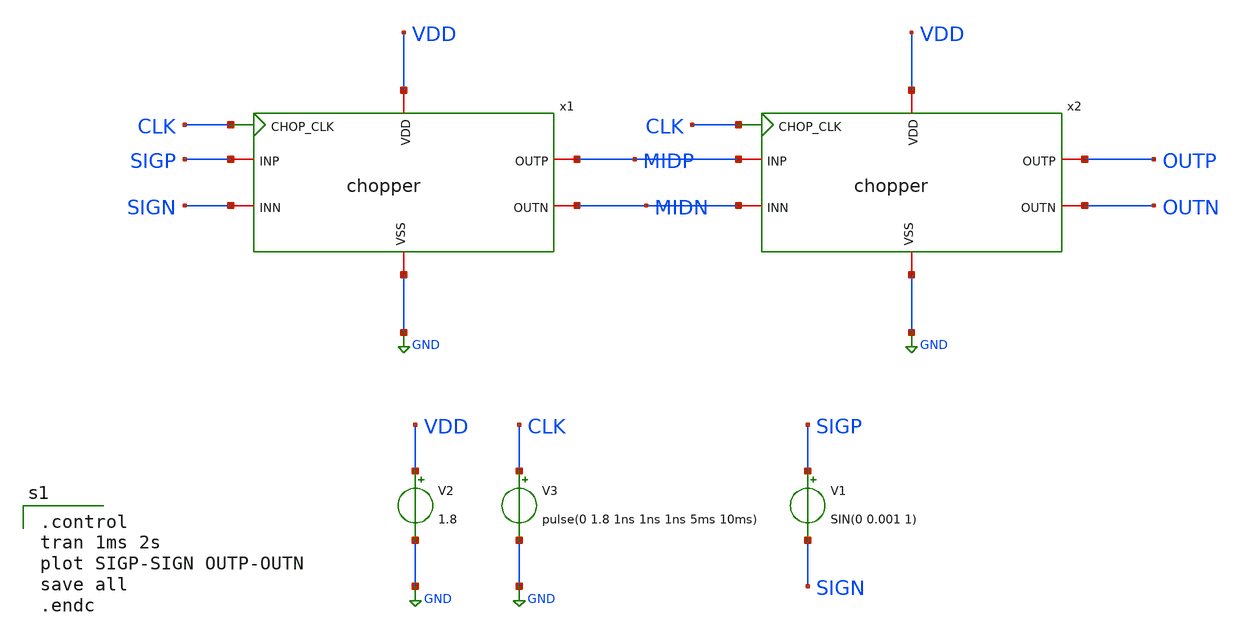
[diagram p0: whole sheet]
** sch_path: opamp_lna/chopper_tb.sch
**.subckt chopper_tb
x1 GND VDD MIDP SIGP CLK MIDN SIGN chopper
V1 SIGP SIGN SIN(0 0.001 1)
V2 VDD GND 1.8
V3 CLK GND pulse(0 1.8 1ns 1ns 1ns 5ms 10ms)
x2 GND VDD OUTP MIDP CLK OUTN MIDN chopper
**** begin user architecture code

** opencircuitdesign pdks install
.lib $::SKYWATER_MODELS/sky130.lib.spice tt
.include $::SKYWATER_STDCELLS/sky130_fd_sc_hd.spice


.control
tran 1ms 2s
plot SIGP-SIGN OUTP-OUTN
save all
.endc

**** end user architecture code
**.ends

* expanding   symbol:  chopper.sym # of pins=7
** sym_path: opamp_lna/chopper.sym
** sch_path: opamp_lna/chopper.sch
.subckt chopper VSS VDD OUTP INP CHOP_CLK OUTN INN
*.ipin CHOP_CLK
*.iopin INP
*.iopin INN
*.iopin OUTP
*.iopin OUTN
*.iopin VSS
*.iopin VDD
XM1 OUTN SWB INP VSS sky130_fd_pr__nfet_01v8 L=0.15 W=2 nf=1 ad='int((nf+1)/2) * W/nf * 0.29' as='int((nf+2)/2) * W/nf * 0.29'
+ pd='2*int((nf+1)/2) * (W/nf + 0.29)' ps='2*int((nf+2)/2) * (W/nf + 0.29)' nrd='0.29 / W' nrs='0.29 / W'
+ sa=0 sb=0 sd=0 mult=1 m=1
XM2 OUTN SW INP VDD sky130_fd_pr__pfet_01v8 L=0.15 W=2 nf=1 ad='int((nf+1)/2) * W/nf * 0.29' as='int((nf+2)/2) * W/nf * 0.29'
+ pd='2*int((nf+1)/2) * (W/nf + 0.29)' ps='2*int((nf+2)/2) * (W/nf + 0.29)' nrd='0.29 / W' nrs='0.29 / W'
+ sa=0 sb=0 sd=0 mult=1 m=1
XM3 OUTP SW INP VSS sky130_fd_pr__nfet_01v8 L=0.15 W=2 nf=1 ad='int((nf+1)/2) * W/nf * 0.29' as='int((nf+2)/2) * W/nf * 0.29'
+ pd='2*int((nf+1)/2) * (W/nf + 0.29)' ps='2*int((nf+2)/2) * (W/nf + 0.29)' nrd='0.29 / W' nrs='0.29 / W'
+ sa=0 sb=0 sd=0 mult=1 m=1
XM4 OUTP SWB INP VDD sky130_fd_pr__pfet_01v8 L=0.15 W=2 nf=1 ad='int((nf+1)/2) * W/nf * 0.29' as='int((nf+2)/2) * W/nf * 0.29'
+ pd='2*int((nf+1)/2) * (W/nf + 0.29)' ps='2*int((nf+2)/2) * (W/nf + 0.29)' nrd='0.29 / W' nrs='0.29 / W'
+ sa=0 sb=0 sd=0 mult=1 m=1
XM5 OUTN SW INN VSS sky130_fd_pr__nfet_01v8 L=0.15 W=2 nf=1 ad='int((nf+1)/2) * W/nf * 0.29' as='int((nf+2)/2) * W/nf * 0.29'
+ pd='2*int((nf+1)/2) * (W/nf + 0.29)' ps='2*int((nf+2)/2) * (W/nf + 0.29)' nrd='0.29 / W' nrs='0.29 / W'
+ sa=0 sb=0 sd=0 mult=1 m=1
XM6 OUTN SWB INN VDD sky130_fd_pr__pfet_01v8 L=0.15 W=2 nf=1 ad='int((nf+1)/2) * W/nf * 0.29' as='int((nf+2)/2) * W/nf * 0.29'
+ pd='2*int((nf+1)/2) * (W/nf + 0.29)' ps='2*int((nf+2)/2) * (W/nf + 0.29)' nrd='0.29 / W' nrs='0.29 / W'
+ sa=0 sb=0 sd=0 mult=1 m=1
XM7 OUTP SWB INN VSS sky130_fd_pr__nfet_01v8 L=0.15 W=2 nf=1 ad='int((nf+1)/2) * W/nf * 0.29' as='int((nf+2)/2) * W/nf * 0.29'
+ pd='2*int((nf+1)/2) * (W/nf + 0.29)' ps='2*int((nf+2)/2) * (W/nf + 0.29)' nrd='0.29 / W' nrs='0.29 / W'
+ sa=0 sb=0 sd=0 mult=1 m=1
XM8 OUTP SW INN VDD sky130_fd_pr__pfet_01v8 L=0.15 W=2 nf=1 ad='int((nf+1)/2) * W/nf * 0.29' as='int((nf+2)/2) * W/nf * 0.29'
+ pd='2*int((nf+1)/2) * (W/nf + 0.29)' ps='2*int((nf+2)/2) * (W/nf + 0.29)' nrd='0.29 / W' nrs='0.29 / W'
+ sa=0 sb=0 sd=0 mult=1 m=1
x5 CHOP_CLK VSS VNB VPB VDD net2 sky130_fd_sc_hd__clkbuf_2
x1 CHOP_CLK VGND VNB VPB VPWR net1 sky130_fd_sc_hd__clkinv_2
x2 net1 VSS VNB VPB VDD SWB sky130_fd_sc_hd__clkinv_8
x3 net2 VSS VNB VPB VDD SW sky130_fd_sc_hd__clkinv_8
.ends

.GLOBAL GND
.end
